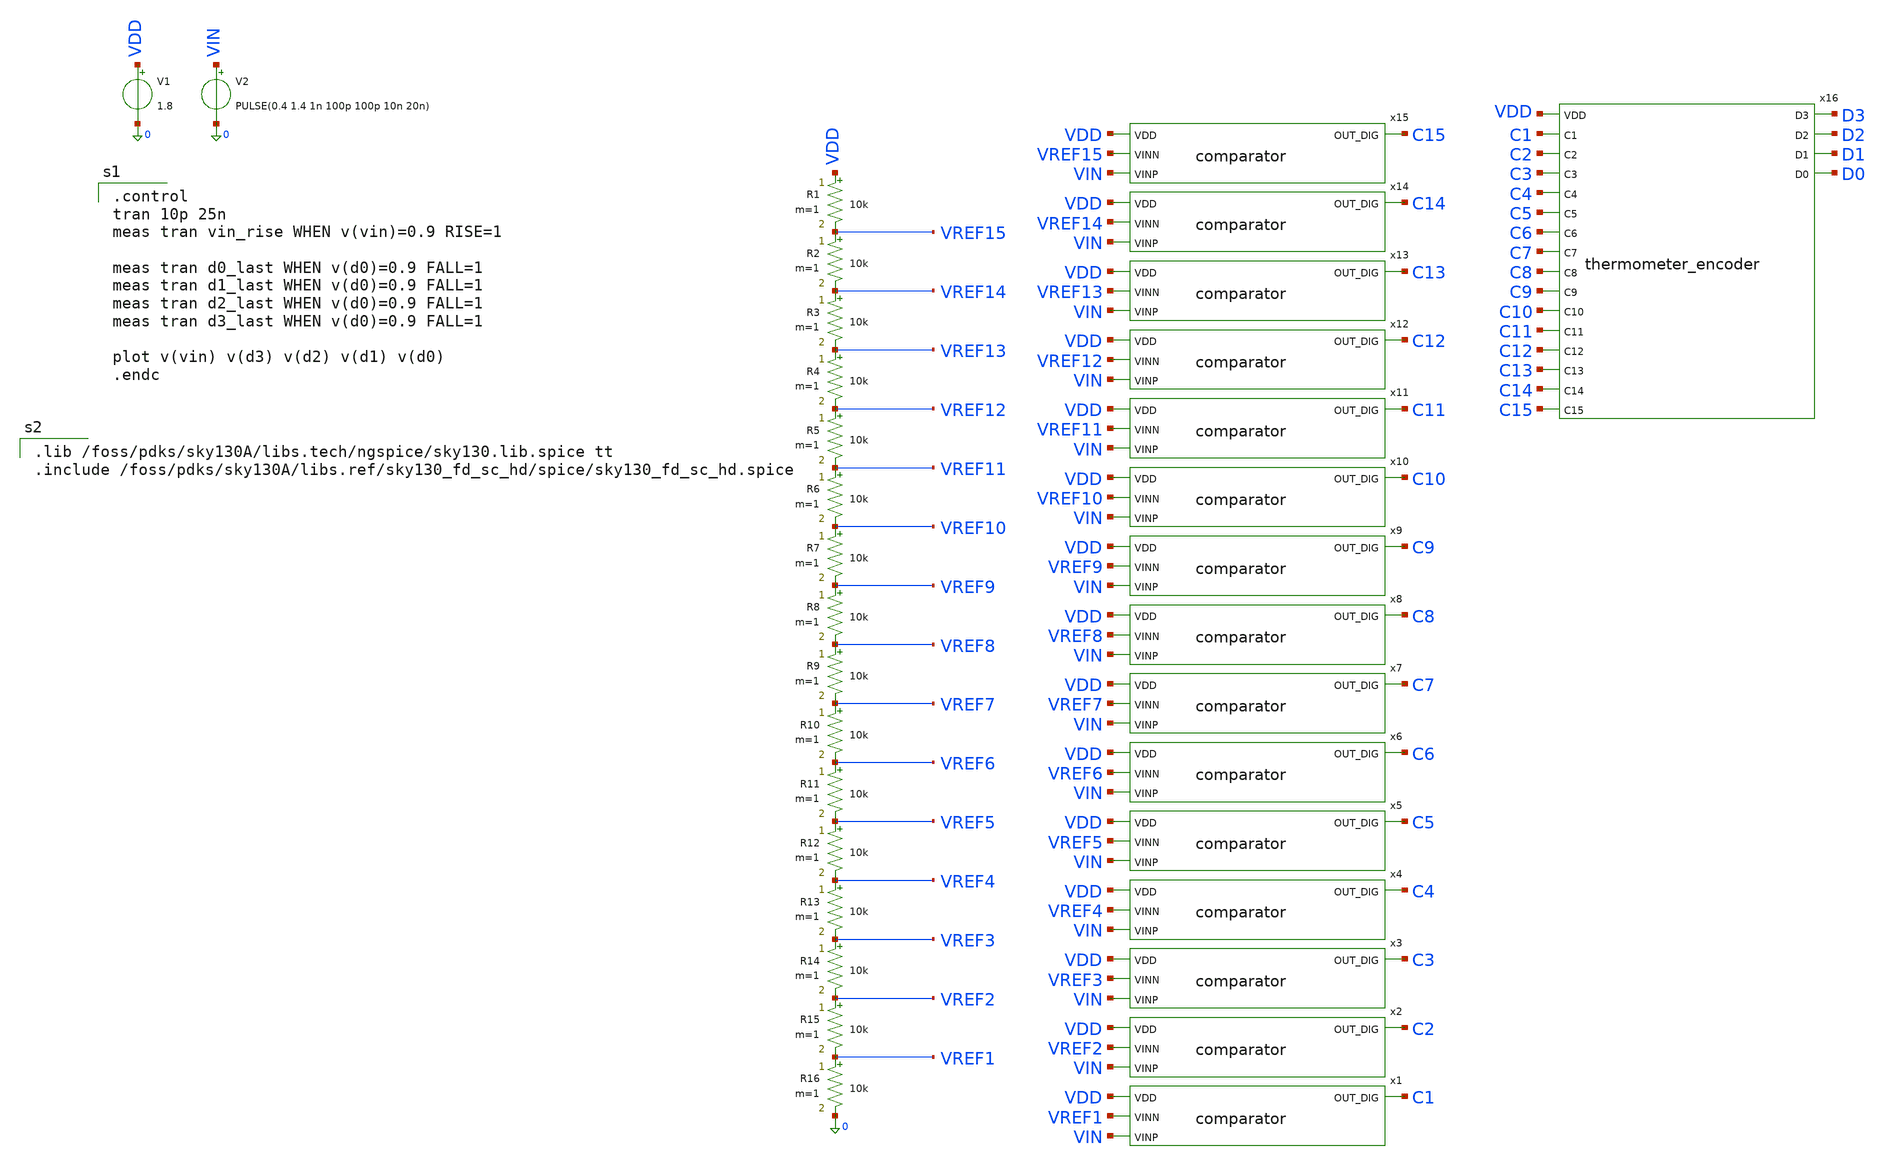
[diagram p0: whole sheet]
** sch_path: flash_adc.sch
**.subckt flash_adc
R1 VDD VREF15 10k m=1
R2 VREF15 VREF14 10k m=1
R3 VREF14 VREF13 10k m=1
R4 VREF13 VREF12 10k m=1
R5 VREF12 VREF11 10k m=1
R6 VREF11 VREF10 10k m=1
R7 VREF10 VREF9 10k m=1
R8 VREF9 VREF8 10k m=1
R9 VREF8 VREF7 10k m=1
R10 VREF7 VREF6 10k m=1
R11 VREF6 VREF5 10k m=1
R12 VREF5 VREF4 10k m=1
R13 VREF4 VREF3 10k m=1
R14 VREF3 VREF2 10k m=1
R15 VREF2 VREF1 10k m=1
R16 VREF1 0 10k m=1
V1 VDD 0 1.8
V2 VIN 0 PULSE(0.4 1.4 1n 100p 100p 10n 20n)
x1 VDD C1 VREF1 VIN comparator
x2 VDD C2 VREF2 VIN comparator
x3 VDD C3 VREF3 VIN comparator
x4 VDD C4 VREF4 VIN comparator
x5 VDD C5 VREF5 VIN comparator
x6 VDD C6 VREF6 VIN comparator
x7 VDD C7 VREF7 VIN comparator
x8 VDD C8 VREF8 VIN comparator
x9 VDD C9 VREF9 VIN comparator
x10 VDD C10 VREF10 VIN comparator
x11 VDD C11 VREF11 VIN comparator
x12 VDD C12 VREF12 VIN comparator
x13 VDD C13 VREF13 VIN comparator
x14 VDD C14 VREF14 VIN comparator
x15 VDD C15 VREF15 VIN comparator
x16 VDD D3 D2 C1 C2 D1 C3 D0 C4 C5 C6 C7 C8 C9 C10 C11 C12 C13 C14 C15 thermometer_encoder
**** begin user architecture code

.control
tran 10p 25n
meas tran vin_rise WHEN v(vin)=0.9 RISE=1

meas tran d0_last WHEN v(d0)=0.9 FALL=1
meas tran d1_last WHEN v(d0)=0.9 FALL=1
meas tran d2_last WHEN v(d0)=0.9 FALL=1
meas tran d3_last WHEN v(d0)=0.9 FALL=1

plot v(vin) v(d3) v(d2) v(d1) v(d0)
.endc


.lib /foss/pdks/sky130A/libs.tech/ngspice/sky130.lib.spice tt
.include /foss/pdks/sky130A/libs.ref/sky130_fd_sc_hd/spice/sky130_fd_sc_hd.spice


**** end user architecture code
**.ends

* expanding   symbol:  comparator.sym # of pins=4
** sym_path: comparator.sym
** sch_path: comparator.sch
.subckt comparator VDD OUT_DIG VINN VINP
*.ipin VINP
*.ipin VINN
*.ipin VDD
*.opin OUT_DIG
I0 net1 0 20uA
XM1 net2 VINP net1 0 sky130_fd_pr__nfet_01v8 L=0.15 W=1 nf=1 ad='int((1 + 1)/2) * 1 / 1 * 0.29' as='int((1 + 2)/2) * 1 / 1 * 0.29'
+ pd='2*int((1 + 1)/2) * (1 / 1 + 0.29)' ps='2*int((1 + 2)/2) * (1 / 1 + 0.29)' nrd='0.29 / 1 ' nrs='0.29 / 1 '
+ sa=0 sb=0 sd=0 mult=1 m=1
XM2 net3 VINN net1 0 sky130_fd_pr__nfet_01v8 L=0.15 W=1 nf=1 ad='int((1 + 1)/2) * 1 / 1 * 0.29' as='int((1 + 2)/2) * 1 / 1 * 0.29'
+ pd='2*int((1 + 1)/2) * (1 / 1 + 0.29)' ps='2*int((1 + 2)/2) * (1 / 1 + 0.29)' nrd='0.29 / 1 ' nrs='0.29 / 1 '
+ sa=0 sb=0 sd=0 mult=1 m=1
XM6 OUT_DIG net3 0 0 sky130_fd_pr__nfet_01v8 L=0.15 W=1 nf=1 ad='int((1 + 1)/2) * 1 / 1 * 0.29' as='int((1 + 2)/2) * 1 / 1 * 0.29'
+ pd='2*int((1 + 1)/2) * (1 / 1 + 0.29)' ps='2*int((1 + 2)/2) * (1 / 1 + 0.29)' nrd='0.29 / 1 ' nrs='0.29 / 1 '
+ sa=0 sb=0 sd=0 mult=1 m=1
XM3 net2 net2 VDD VDD sky130_fd_pr__pfet_01v8 L=0.15 W=1 nf=1 ad='int((1 + 1)/2) * 1 / 1 * 0.29' as='int((1 + 2)/2) * 1 / 1 * 0.29'
+ pd='2*int((1 + 1)/2) * (1 / 1 + 0.29)' ps='2*int((1 + 2)/2) * (1 / 1 + 0.29)' nrd='0.29 / 1 ' nrs='0.29 / 1 '
+ sa=0 sb=0 sd=0 mult=1 m=1
XM4 net3 net2 VDD VDD sky130_fd_pr__pfet_01v8 L=0.15 W=1 nf=1 ad='int((1 + 1)/2) * 1 / 1 * 0.29' as='int((1 + 2)/2) * 1 / 1 * 0.29'
+ pd='2*int((1 + 1)/2) * (1 / 1 + 0.29)' ps='2*int((1 + 2)/2) * (1 / 1 + 0.29)' nrd='0.29 / 1 ' nrs='0.29 / 1 '
+ sa=0 sb=0 sd=0 mult=1 m=1
XM5 OUT_DIG net3 VDD VDD sky130_fd_pr__pfet_01v8 L=0.15 W=1 nf=1 ad='int((1 + 1)/2) * 1 / 1 * 0.29' as='int((1 + 2)/2) * 1 / 1 * 0.29'
+ pd='2*int((1 + 1)/2) * (1 / 1 + 0.29)' ps='2*int((1 + 2)/2) * (1 / 1 + 0.29)' nrd='0.29 / 1 ' nrs='0.29 / 1 '
+ sa=0 sb=0 sd=0 mult=1 m=1
.ends


* expanding   symbol:  thermometer_encoder.sym # of pins=20
** sym_path: thermometer_encoder.sym
** sch_path: thermometer_encoder.sch
.subckt thermometer_encoder VDD D3 D2 C1 C2 D1 C3 D0 C4 C5 C6 C7 C8 C9 C10 C11 C12 C13 C14 C15
*.ipin C1
*.opin D0
*.ipin C2
*.ipin C3
*.ipin C4
*.ipin C5
*.ipin C6
*.ipin C7
*.ipin C8
*.ipin C9
*.ipin C10
*.ipin C11
*.ipin C12
*.ipin C13
*.ipin C14
*.ipin C15
*.opin D1
*.opin D2
*.opin D3
*.ipin VDD
x1 C8 0 0 VDD VDD D3 sky130_fd_sc_hd__inv_1
x2 C4 0 0 VDD VDD net27 sky130_fd_sc_hd__inv_1
x3 C12 0 0 VDD VDD net2 sky130_fd_sc_hd__inv_1
x4 net27 C8 0 0 VDD VDD net1 sky130_fd_sc_hd__and2_1
x5 net1 net2 0 0 VDD VDD D2 sky130_fd_sc_hd__or2_1
x6 C2 0 0 VDD VDD net7 sky130_fd_sc_hd__inv_1
x7 C10 0 0 VDD VDD net9 sky130_fd_sc_hd__inv_1
x8 C6 0 0 VDD VDD net8 sky130_fd_sc_hd__inv_1
x9 C14 0 0 VDD VDD net6 sky130_fd_sc_hd__inv_1
x12 net9 C12 0 0 VDD VDD net5 sky130_fd_sc_hd__and2_1
x13 net3 net4 net5 net6 0 0 VDD VDD D1 sky130_fd_sc_hd__or4_1
x10 net8 C8 0 0 VDD VDD net4 sky130_fd_sc_hd__and2_1
x11 net7 C4 0 0 VDD VDD net3 sky130_fd_sc_hd__and2_1
x15 C13 0 0 VDD VDD net16 sky130_fd_sc_hd__inv_1
x17 C11 0 0 VDD VDD net15 sky130_fd_sc_hd__inv_1
x18 C15 0 0 VDD VDD net24 sky130_fd_sc_hd__inv_1
x19 C9 0 0 VDD VDD net14 sky130_fd_sc_hd__inv_1
x20 C1 0 0 VDD VDD net10 sky130_fd_sc_hd__inv_1
x21 C3 0 0 VDD VDD net11 sky130_fd_sc_hd__inv_1
x22 net16 C14 0 0 VDD VDD net23 sky130_fd_sc_hd__and2_1
x23 net14 C10 0 0 VDD VDD net21 sky130_fd_sc_hd__and2_1
x24 net11 C4 0 0 VDD VDD net18 sky130_fd_sc_hd__and2_1
x25 net10 C2 0 0 VDD VDD net17 sky130_fd_sc_hd__and2_1
x26 net15 C12 0 0 VDD VDD net22 sky130_fd_sc_hd__and2_1
x27 net13 C8 0 0 VDD VDD net20 sky130_fd_sc_hd__and2_1
x28 net12 C6 0 0 VDD VDD net19 sky130_fd_sc_hd__and2_1
x29 net17 net18 net19 net20 0 0 VDD VDD net25 sky130_fd_sc_hd__or4_1
x30 net21 net22 net23 net24 0 0 VDD VDD net26 sky130_fd_sc_hd__or4_1
x31 net25 net26 0 0 VDD VDD D0 sky130_fd_sc_hd__or2_1
x32 C5 0 0 VDD VDD net12 sky130_fd_sc_hd__inv_1
x33 C7 0 0 VDD VDD net13 sky130_fd_sc_hd__inv_1
.ends

.end
